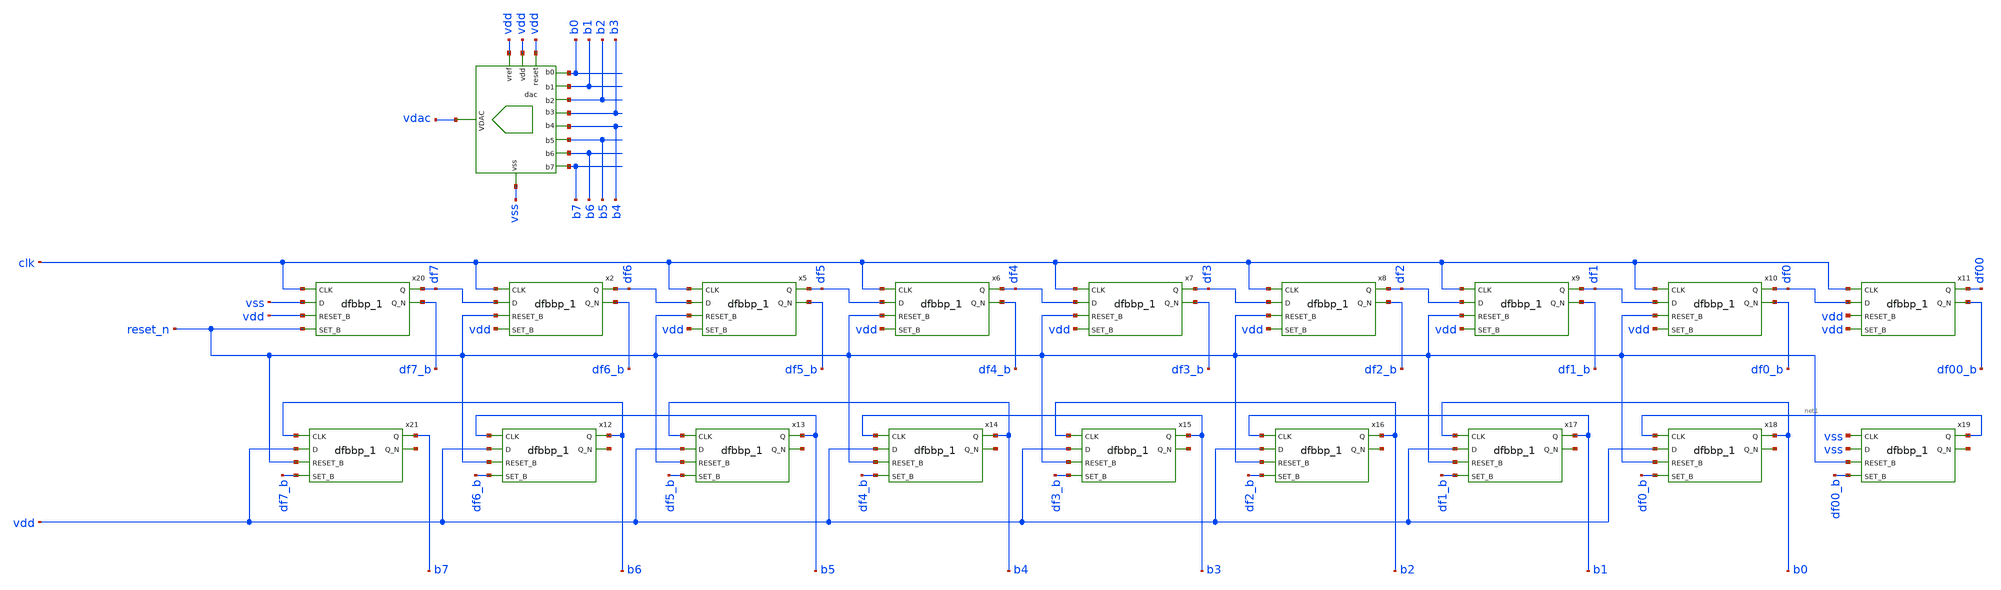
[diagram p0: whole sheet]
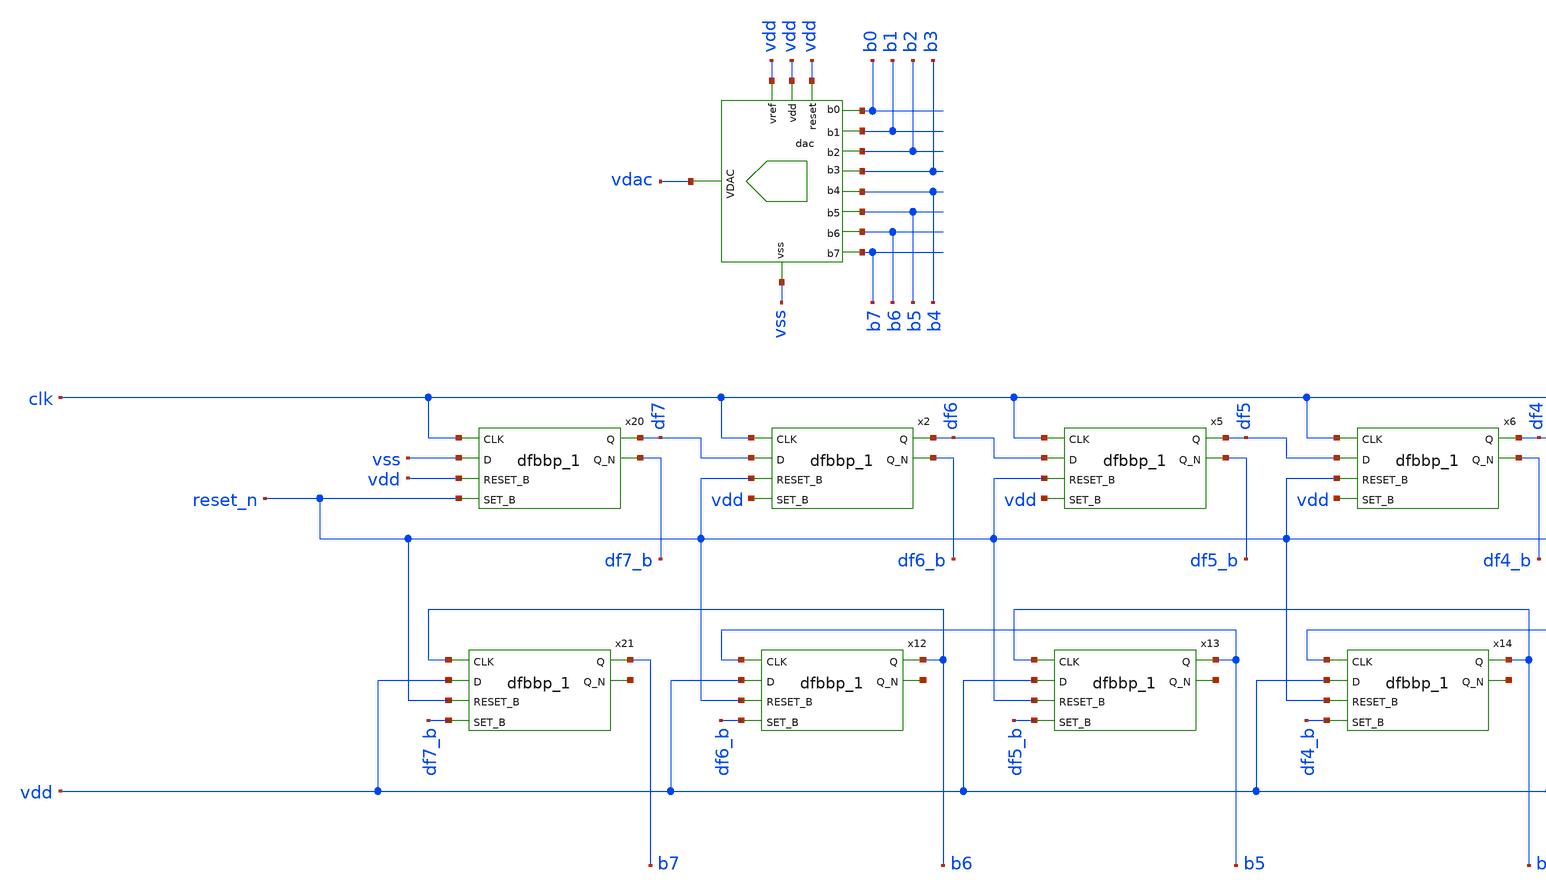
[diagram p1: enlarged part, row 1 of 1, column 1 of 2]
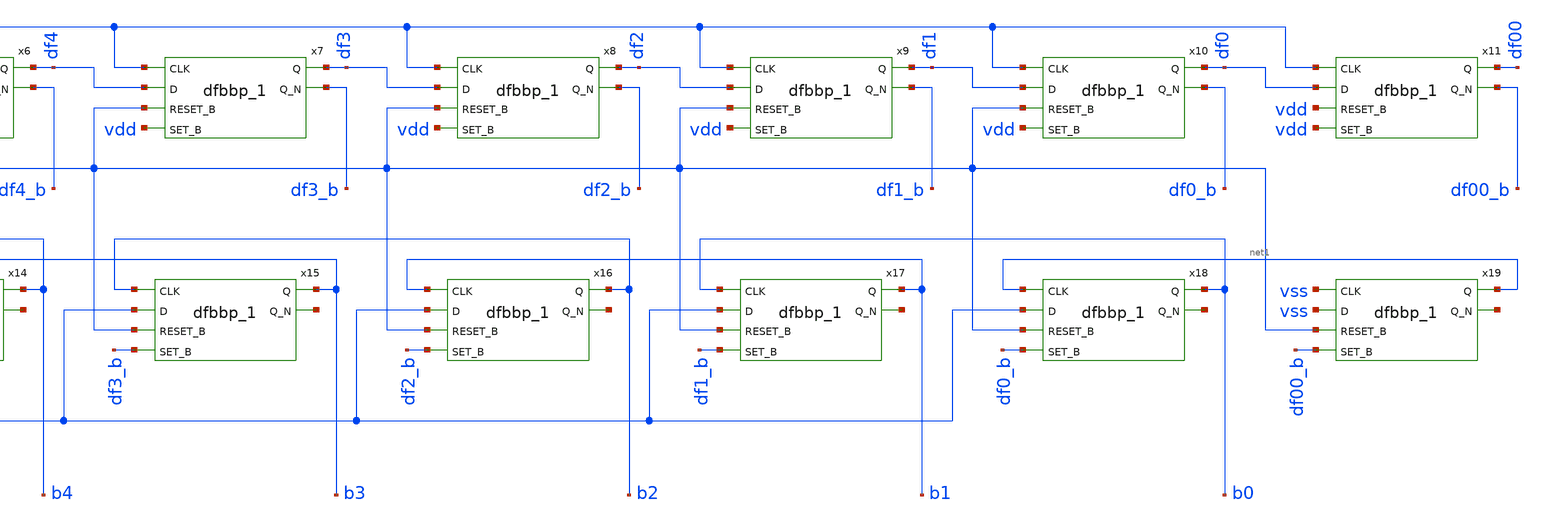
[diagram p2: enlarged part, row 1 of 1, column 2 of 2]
** sch_path: untitled-5.sch
**.subckt untitled-5
x2 clk df7 reset_n vdd vss vss vdd vdd df6 df6_b sky130_fd_sc_hd__dfbbp_1
x5 clk df6 reset_n vdd vss vss vdd vdd df5 df5_b sky130_fd_sc_hd__dfbbp_1
x6 clk df5 reset_n vdd vss vss vdd vdd df4 df4_b sky130_fd_sc_hd__dfbbp_1
x7 clk df4 reset_n vdd vss vss vdd vdd df3 df3_b sky130_fd_sc_hd__dfbbp_1
x8 clk df3 reset_n vdd vss vss vdd vdd df2 df2_b sky130_fd_sc_hd__dfbbp_1
x9 clk df2 reset_n vdd vss vss vdd vdd df1 df1_b sky130_fd_sc_hd__dfbbp_1
x10 clk df1 reset_n vdd vss vss vdd vdd df0 df0_b sky130_fd_sc_hd__dfbbp_1
x11 clk df0 vdd vdd vss vss vdd vdd df00 df00_b sky130_fd_sc_hd__dfbbp_1
x12 b5 vdd reset_n df6_b vss vss vdd vdd b6 net2 sky130_fd_sc_hd__dfbbp_1
x13 b4 vdd reset_n df5_b vss vss vdd vdd b5 net3 sky130_fd_sc_hd__dfbbp_1
x14 b3 vdd reset_n df4_b vss vss vdd vdd b4 net4 sky130_fd_sc_hd__dfbbp_1
x15 b2 vdd reset_n df3_b vss vss vdd vdd b3 net5 sky130_fd_sc_hd__dfbbp_1
x16 b1 vdd reset_n df2_b vss vss vdd vdd b2 net6 sky130_fd_sc_hd__dfbbp_1
x17 b0 vdd reset_n df1_b vss vss vdd vdd b1 net7 sky130_fd_sc_hd__dfbbp_1
x18 net1 vdd reset_n df0_b vss vss vdd vdd b0 net8 sky130_fd_sc_hd__dfbbp_1
x19 vss vss reset_n df00_b vss vss vdd vdd net1 net9 sky130_fd_sc_hd__dfbbp_1
x20 clk vss vdd reset_n vss vss vdd vdd df7 df7_b sky130_fd_sc_hd__dfbbp_1
x21 b6 vdd reset_n df7_b vss vss vdd vdd b7 net10 sky130_fd_sc_hd__dfbbp_1
X1 vss vdac vdd vdd b0 b1 b2 b3 b4 b5 b6 b7 vdd dac
**.ends

* expanding   symbol:  xschem/dac/dac.sym # of pins=13
** sym_path: xschem/dac/dac.sym
** sch_path: xschem/dac/dac.sch
.subckt dac vss vdac vdd vref s0 s1 s2 s3 s4 s5 s6 s7 reset
*.ipin s7
*.ipin s6
*.ipin s5
*.ipin s4
*.ipin s3
*.ipin s2
*.ipin s1
*.ipin s0
*.iopin vdd
*.iopin vss
*.iopin vref
*.opin vdac
*.ipin reset
XC2 net1 net2 sky130_fd_pr__cap_mim_m3_1 W=w L=l MF=8 m=8
X2 net2 vref vss vdd net14 vss dac_sw
XC1 net1 net3 sky130_fd_pr__cap_mim_m3_1 W=w L=l MF=4 m=4
X3 net3 vref vss vdd net15 vss dac_sw
X4 net4 vref vss vdd net16 vss dac_sw
X5 net5 vref vss vdd net17 vss dac_sw
XC3 net1 net4 sky130_fd_pr__cap_mim_m3_1 W=w L=l MF=2 m=2
XC4 net1 net5 sky130_fd_pr__cap_mim_m3_1 W=w L=l MF=1 m=1
XC5 vss net1 sky130_fd_pr__cap_mim_m3_1 W=w L=l MF=1 m=1
X1 net6 vref vss vdd net13 vss dac_sw
X6 net7 vref vss vdd net12 vss dac_sw
X7 net8 vref vss vdd net11 vss dac_sw
X8 net9 vref vss vdd net10 vss dac_sw
x9 vss s7 reset vss vss vdd vdd net10 sky130_fd_sc_hd__mux2_1
x10 vss s6 reset vss vss vdd vdd net11 sky130_fd_sc_hd__mux2_1
x11 vss s5 reset vss vss vdd vdd net12 sky130_fd_sc_hd__mux2_1
x12 vss s4 reset vss vss vdd vdd net13 sky130_fd_sc_hd__mux2_1
x13 vss s3 reset vss vss vdd vdd net14 sky130_fd_sc_hd__mux2_1
x14 vss s2 reset vss vss vdd vdd net15 sky130_fd_sc_hd__mux2_1
x15 vss s1 reset vss vss vdd vdd net16 sky130_fd_sc_hd__mux2_1
x16 vss s0 reset vss vss vdd vdd net17 sky130_fd_sc_hd__mux2_1
XM1 vdac net18 vss vss sky130_fd_pr__nfet_01v8 L=0.15 W=5 nf=1 ad='int((nf+1)/2) * W/nf * 0.29' as='int((nf+2)/2) * W/nf * 0.29'
+ pd='2*int((nf+1)/2) * (W/nf + 0.29)' ps='2*int((nf+2)/2) * (W/nf + 0.29)' nrd='0.29 / W' nrs='0.29 / W'
+ sa=0 sb=0 sd=0 mult=1 m=1
x17 reset vss vss vdd vdd net18 sky130_fd_sc_hd__inv_1
XC10 net1 vdac sky130_fd_pr__cap_mim_m3_1 W=w L=l MF=8/7 m=8/7
XC6 vdac net9 sky130_fd_pr__cap_mim_m3_1 W=w L=l MF=8 m=8
XC7 vdac net8 sky130_fd_pr__cap_mim_m3_1 W=w L=l MF=4 m=4
XC8 vdac net7 sky130_fd_pr__cap_mim_m3_1 W=w L=l MF=2 m=2
XC9 vdac net6 sky130_fd_pr__cap_mim_m3_1 W=w L=l MF=1 m=1
.ends


* expanding   symbol:  xschem/dac/dac_sw.sym # of pins=6
** sym_path: xschem/dac/dac_sw.sym
** sch_path: xschem/dac/dac_sw.sch
.subckt dac_sw c b vss vdd clk a
*.iopin vdd
*.iopin vss
*.ipin clk
*.iopin c
*.iopin a
*.iopin b
XM2 c clk b vss sky130_fd_pr__nfet_01v8 L=0.15 W=10 nf=1 ad='int((nf+1)/2) * W/nf * 0.29' as='int((nf+2)/2) * W/nf * 0.29'
+ pd='2*int((nf+1)/2) * (W/nf + 0.29)' ps='2*int((nf+2)/2) * (W/nf + 0.29)' nrd='0.29 / W' nrs='0.29 / W'
+ sa=0 sb=0 sd=0 mult=1 m=1
XM5 b net1 c vdd sky130_fd_pr__pfet_01v8 L=0.15 W=20 nf=1 ad='int((nf+1)/2) * W/nf * 0.29' as='int((nf+2)/2) * W/nf * 0.29'
+ pd='2*int((nf+1)/2) * (W/nf + 0.29)' ps='2*int((nf+2)/2) * (W/nf + 0.29)' nrd='0.29 / W' nrs='0.29 / W'
+ sa=0 sb=0 sd=0 mult=1 m=1
XM6 c net1 a vss sky130_fd_pr__nfet_01v8 L=0.15 W=10 nf=1 ad='int((nf+1)/2) * W/nf * 0.29' as='int((nf+2)/2) * W/nf * 0.29'
+ pd='2*int((nf+1)/2) * (W/nf + 0.29)' ps='2*int((nf+2)/2) * (W/nf + 0.29)' nrd='0.29 / W' nrs='0.29 / W'
+ sa=0 sb=0 sd=0 mult=1 m=1
XM7 a clk c vdd sky130_fd_pr__pfet_01v8 L=0.15 W=20 nf=1 ad='int((nf+1)/2) * W/nf * 0.29' as='int((nf+2)/2) * W/nf * 0.29'
+ pd='2*int((nf+1)/2) * (W/nf + 0.29)' ps='2*int((nf+2)/2) * (W/nf + 0.29)' nrd='0.29 / W' nrs='0.29 / W'
+ sa=0 sb=0 sd=0 mult=1 m=1
x1 clk vss vss vdd vdd net1 sky130_fd_sc_hd__inv_1
.ends

.end
